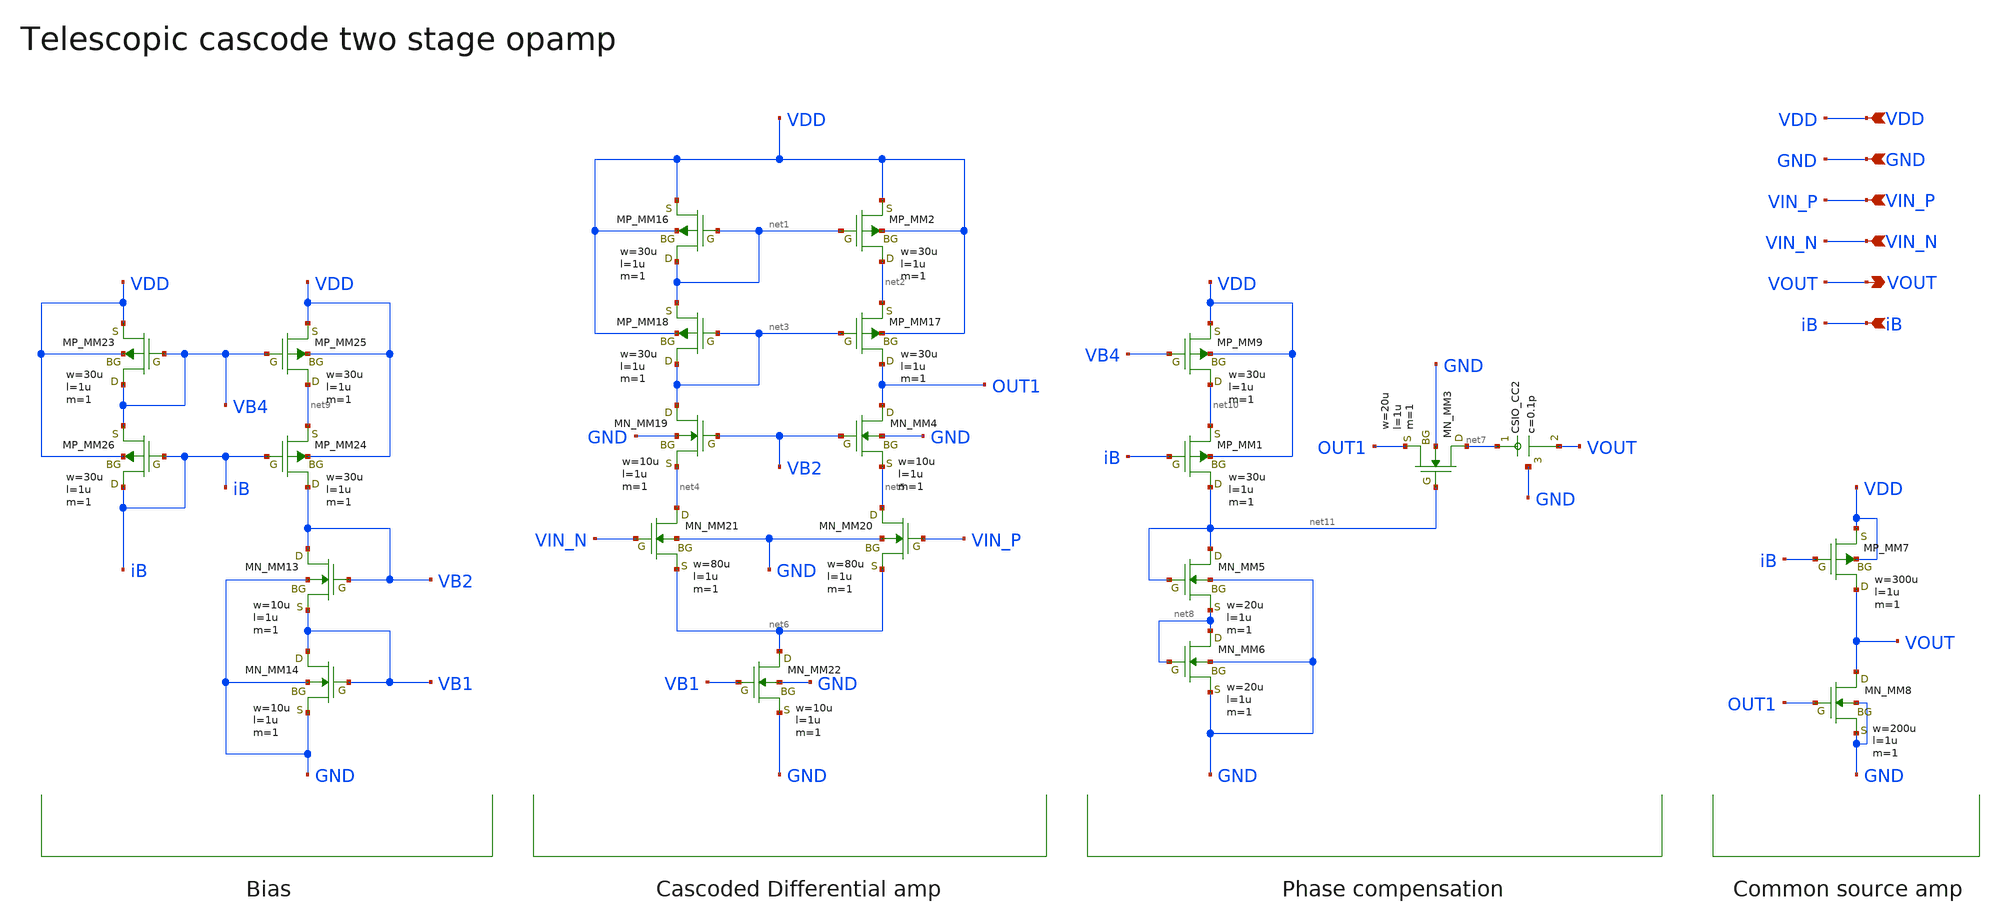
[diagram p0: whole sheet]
** sch_path: member_project/AM_Radio/Yamada3/xschem/cascode_opamp.sch
**.subckt cascode_opamp VOUT VIN_N VIN_P GND VDD iB
*.opin VOUT
*.ipin VIN_N
*.ipin VIN_P
*.ipin GND
*.ipin VDD
*.ipin iB
MM2 net2 net1 VDD VDD PMOS w=30u l=1u as=0 ad=0 ps=0 pd=0 nrd=0 nrs=0 m=1
MM4 OUT1 VB2 net5 GND NMOS w=10u l=1u as=0 ad=0 ps=0 pd=0 nrd=0 nrs=0 m=1
MM7 VOUT iB VDD VDD PMOS w=300u l=1u as=0 ad=0 ps=0 pd=0 nrd=0 nrs=0 m=1
MM8 VOUT OUT1 GND GND NMOS w=200u l=1u as=0 ad=0 ps=0 pd=0 nrd=0 nrs=0 m=1
MM16 net1 net1 VDD VDD PMOS w=30u l=1u as=0 ad=0 ps=0 pd=0 nrd=0 nrs=0 m=1
MM17 OUT1 net3 net2 VDD PMOS w=30u l=1u as=0 ad=0 ps=0 pd=0 nrd=0 nrs=0 m=1
MM18 net3 net3 net1 VDD PMOS w=30u l=1u as=0 ad=0 ps=0 pd=0 nrd=0 nrs=0 m=1
MM19 net3 VB2 net4 GND NMOS w=10u l=1u as=0 ad=0 ps=0 pd=0 nrd=0 nrs=0 m=1
MM20 net5 VIN_P net6 GND NMOS w=80u l=1u as=0 ad=0 ps=0 pd=0 nrd=0 nrs=0 m=1
MM21 net4 VIN_N net6 GND NMOS w=80u l=1u as=0 ad=0 ps=0 pd=0 nrd=0 nrs=0 m=1
MM22 net6 VB1 GND GND NMOS w=10u l=1u as=0 ad=0 ps=0 pd=0 nrd=0 nrs=0 m=1
MM3 net7 net11 OUT1 GND NMOS w=20u l=1u as=0 ad=0 ps=0 pd=0 nrd=0 nrs=0 m=1
CC2 net7 VOUT GND F_CSIO c=0.1p x=120u y=120u m=1
MM5 net11 net11 net8 GND NMOS w=20u l=1u as=0 ad=0 ps=0 pd=0 nrd=0 nrs=0 m=1
MM6 net8 net8 GND GND NMOS w=20u l=1u as=0 ad=0 ps=0 pd=0 nrd=0 nrs=0 m=1
MM13 VB2 VB2 VB1 GND NMOS w=10u l=1u as=0 ad=0 ps=0 pd=0 nrd=0 nrs=0 m=1
MM14 VB1 VB1 GND GND NMOS w=10u l=1u as=0 ad=0 ps=0 pd=0 nrd=0 nrs=0 m=1
MM23 VB4 VB4 VDD VDD PMOS w=30u l=1u as=0 ad=0 ps=0 pd=0 nrd=0 nrs=0 m=1
MM24 VB2 iB net9 VDD PMOS w=30u l=1u as=0 ad=0 ps=0 pd=0 nrd=0 nrs=0 m=1
MM25 net9 VB4 VDD VDD PMOS w=30u l=1u as=0 ad=0 ps=0 pd=0 nrd=0 nrs=0 m=1
MM26 iB iB VB4 VDD PMOS w=30u l=1u as=0 ad=0 ps=0 pd=0 nrd=0 nrs=0 m=1
MM1 net11 iB net10 VDD PMOS w=30u l=1u as=0 ad=0 ps=0 pd=0 nrd=0 nrs=0 m=1
MM9 net10 VB4 VDD VDD PMOS w=30u l=1u as=0 ad=0 ps=0 pd=0 nrd=0 nrs=0 m=1
**.ends
.end
